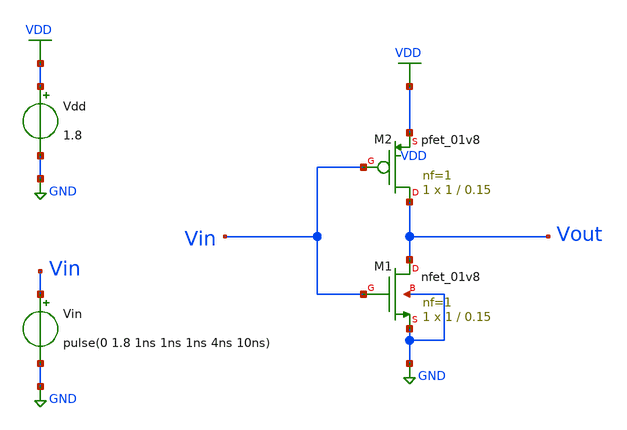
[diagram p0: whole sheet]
** sch_path: projects/inverter_tutorial/xschem_ngspice/inverter_tran.sch
**.subckt inverter_tran
XM1 Vout Vin GND GND sky130_fd_pr__nfet_01v8 L=0.15 W=1 nf=1 ad='int((nf+1)/2) * W/nf * 0.29' as='int((nf+2)/2) * W/nf * 0.29'
+ pd='2*int((nf+1)/2) * (W/nf + 0.29)' ps='2*int((nf+2)/2) * (W/nf + 0.29)' nrd='0.29 / W' nrs='0.29 / W'
+ sa=0 sb=0 sd=0 mult=1 m=1
XM2 Vout Vin VDD VDD sky130_fd_pr__pfet_01v8 L=0.15 W=1 nf=1 ad='int((nf+1)/2) * W/nf * 0.29' as='int((nf+2)/2) * W/nf * 0.29'
+ pd='2*int((nf+1)/2) * (W/nf + 0.29)' ps='2*int((nf+2)/2) * (W/nf + 0.29)' nrd='0.29 / W' nrs='0.29 / W'
+ sa=0 sb=0 sd=0 mult=1 m=1
Vin Vin GND pulse(0 1.8 1ns 1ns 1ns 4ns 10ns)
Vdd VDD GND 1.8
**** begin user architecture code



.lib /foss/pdks/sky130A/libs.tech/ngspice/sky130.lib.spice tt

.tran 0.01n 1u

.save all



**** end user architecture code
**.ends
.GLOBAL VDD
.GLOBAL GND
.end
